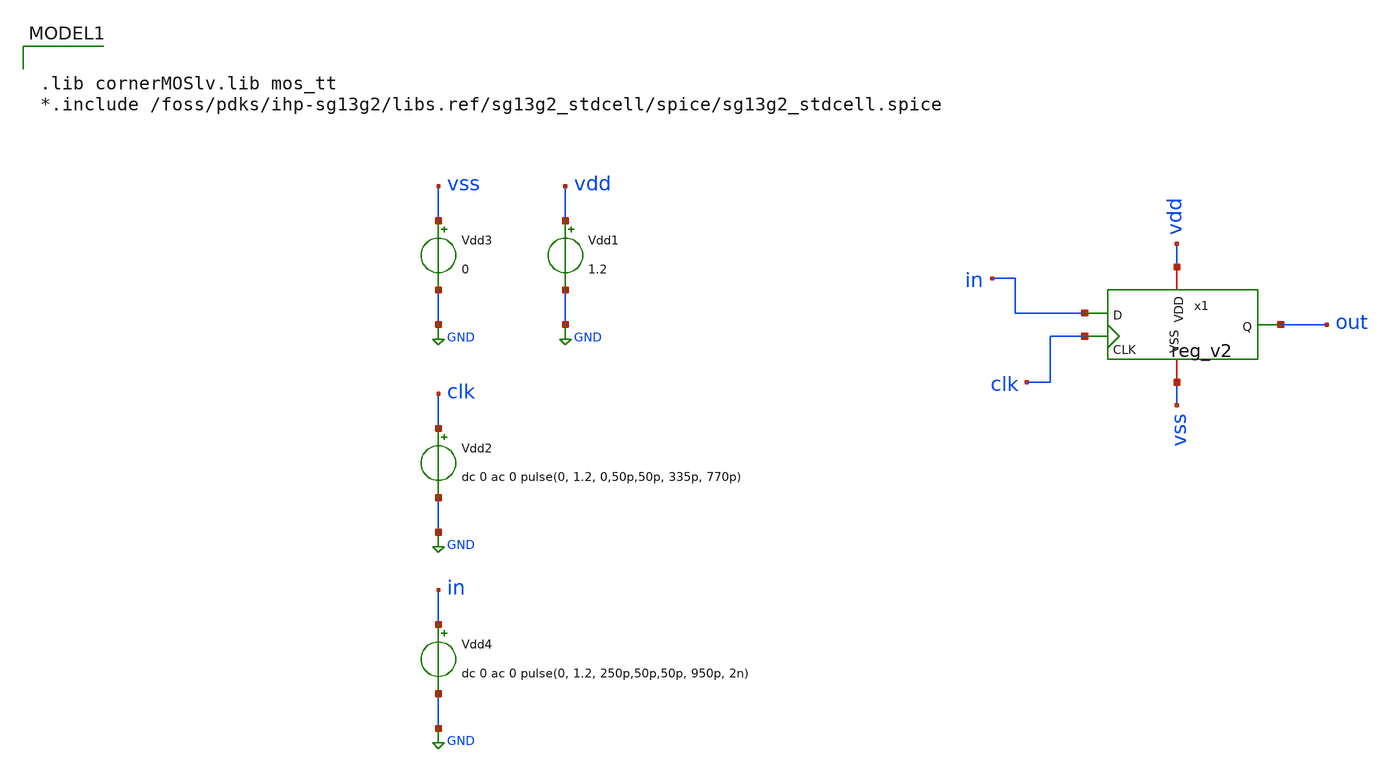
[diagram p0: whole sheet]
** sch_path: Custom_std_cells/tb_reg.sch
**.subckt tb_reg
Vdd1 vdd GND 1.2
Vdd3 vss GND 0
Vdd2 clk GND dc 0 ac 0 pulse(0, 1.2, 0,50p,50p, 335p, 770p)
Vdd4 in GND dc 0 ac 0 pulse(0, 1.2, 250p,50p,50p, 950p, 2n)
x1 vdd clk vss out in reg_v2
**** begin user architecture code

.lib cornerMOSlv.lib mos_tt
*.include /foss/pdks/ihp-sg13g2/libs.ref/sg13g2_stdcell/spice/sg13g2_stdcell.spice




.save v(clk) v(in) v(out)


.tran 5p 6n

.control
run
set color0=white
write tran_logic.raw

.endc


**** end user architecture code
**.ends

* expanding   symbol:  reg_v2.sym # of pins=5
** sym_path: reg_v2.sym
** sch_path: reg_v2.sch
.subckt reg_v2 VDD CLK VSS Q D
*.iopin VDD
*.iopin VSS
*.ipin CLK
*.ipin D
*.opin Q
x3 net7 CLK CLK_B net2 VDD VSS tg_custom
x9 VDD CLK_B CLK VSS inv
x4 VDD net2 net1 VSS inv
x8 VDD net4 D VSS inv
x11 VDD net3 Q VSS inv
x10 VDD net5 net1 VSS inv
x2 net7 CLK_B CLK net4 VDD VSS tg_custom
x6 net6 CLK_B CLK net3 VDD VSS tg_custom
x7 net6 CLK CLK_B net5 VDD VSS tg_custom
x5 VDD net1 net7 VSS inv
x1 VDD Q net6 VSS inv
.ends


* expanding   symbol:  /foss/designs/PhaseInterpolator/Custom_std_Cells/tg_custom.sym # of pins=6
** sym_path: /foss/designs/PhaseInterpolator/Custom_std_Cells/tg_custom.sym
** sch_path: /foss/designs/PhaseInterpolator/Custom_std_Cells/tg_custom.sch
.subckt tg_custom VOUT VSN VSP VIN VBP VBN
*.iopin VIN
*.iopin VSN
*.iopin VOUT
*.iopin VSP
*.iopin VBN
*.iopin VBP
XM1 VOUT VSN VIN VBN sg13_lv_nmos w=0.15u l=0.13u ng=1 m=1 mm_ok=1
XM2 VOUT VSP VIN VBP sg13_lv_pmos w=0.15u l=0.13u ng=1 m=2 mm_ok=1
.ends

.GLOBAL GND
.end
